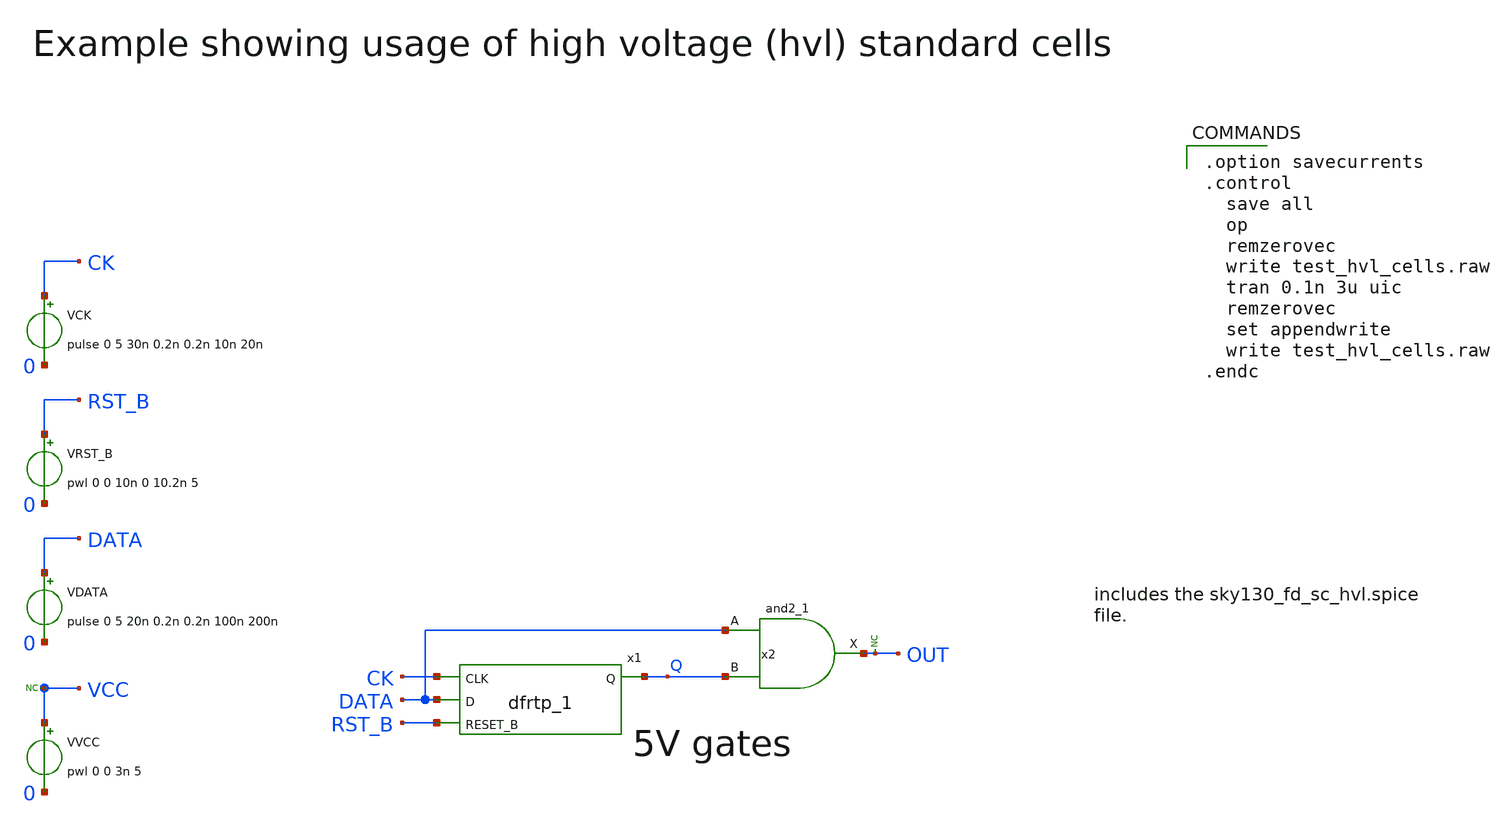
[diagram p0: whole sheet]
** sch_path: sky130A/xschem_libs/sky130_tests/test_hvl_cells/schematic/test_hvl_cells.sch
* Copyright 2021 Stefan Frederik Schippers
* Licensed under the Apache License, Version 2.0 (the "License");
* you may not use this file except in compliance with the License.
* You may obtain a copy of the License at
* https://www.apache.org/licenses/LICENSE-2.0
* Unless required by applicable law or agreed to in writing, software
* distributed under the License is distributed on an "AS IS" BASIS,
* WITHOUT WARRANTIES OR CONDITIONS OF ANY KIND, either express or implied.
* See the License for the specific language governing permissions and
* limitations under the License.
.lib $::SKYWATER_MODELS/sky130.lib.spice tt
.include $PDK_ROOT/$PDK/libs.ref/sky130_fd_sc_hvl/spice/sky130_fd_sc_hvl.spice

**.subckt test_hvl_cells
VVCC VCC 0 pwl 0 0 3n 5
x1 CK DATA RST_B 0 0 VCC VCC Q sky130_fd_sc_hvl__dfrtp_1
x2 DATA Q 0 0 VCC VCC OUT sky130_fd_sc_hvl__and2_1
VCK CK 0 pulse 0 5 30n 0.2n 0.2n 10n 20n
VDATA DATA 0 pulse 0 5 20n 0.2n 0.2n 100n 200n
VRST_B RST_B 0 pwl 0 0 10n 0 10.2n 5
* noconn VCC
* noconn OUT
**** begin user architecture code

.option savecurrents
.control
  save all
  op
  remzerovec
  write test_hvl_cells.raw
  tran 0.1n 3u uic
  remzerovec
  set appendwrite
  write test_hvl_cells.raw
.endc


**** end user architecture code
**.ends
.end
